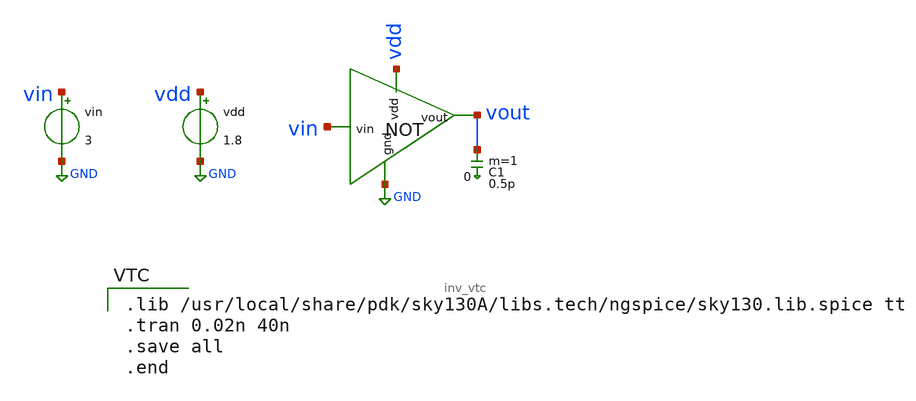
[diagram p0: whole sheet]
** sch_path: Xshem_files/inv_test_delay.sch
**.subckt inv_test_delay
x1 vdd vin GND vout inv_vtc
vin vin GND 3
vdd vdd GND 1.8
C1 vout 0 0.5p m=1
**** begin user architecture code

.lib /usr/local/share/pdk/sky130A/libs.tech/ngspice/sky130.lib.spice tt
.tran 0.02n 40n
.save all
.end

**** end user architecture code
**.ends

* expanding   symbol:  inv_vtc.sym # of pins=4
** sym_path: Xshem_files/inv_vtc.sym
** sch_path: Xshem_files/inv_vtc.sch
.subckt inv_vtc vdd vin gnd vout
*.ipin vin
*.ipin vdd
*.ipin gnd
*.opin vout
XM2 vout vin vdd vdd sky130_fd_pr__pfet_01v8 L=0.15 W=2 nf=1 ad='int((nf+1)/2) * W/nf * 0.29' as='int((nf+2)/2) * W/nf * 0.29'
+ pd='2*int((nf+1)/2) * (W/nf + 0.29)' ps='2*int((nf+2)/2) * (W/nf + 0.29)' nrd='0.29 / W' nrs='0.29 / W'
+ sa=0 sb=0 sd=0 mult=1 m=1
XM1 vout vin gnd gnd sky130_fd_pr__nfet_01v8 L=0.15 W=1 nf=1 ad='int((nf+1)/2) * W/nf * 0.29' as='int((nf+2)/2) * W/nf * 0.29'
+ pd='2*int((nf+1)/2) * (W/nf + 0.29)' ps='2*int((nf+2)/2) * (W/nf + 0.29)' nrd='0.29 / W' nrs='0.29 / W'
+ sa=0 sb=0 sd=0 mult=1 m=1
.ends

.GLOBAL GND
.end
